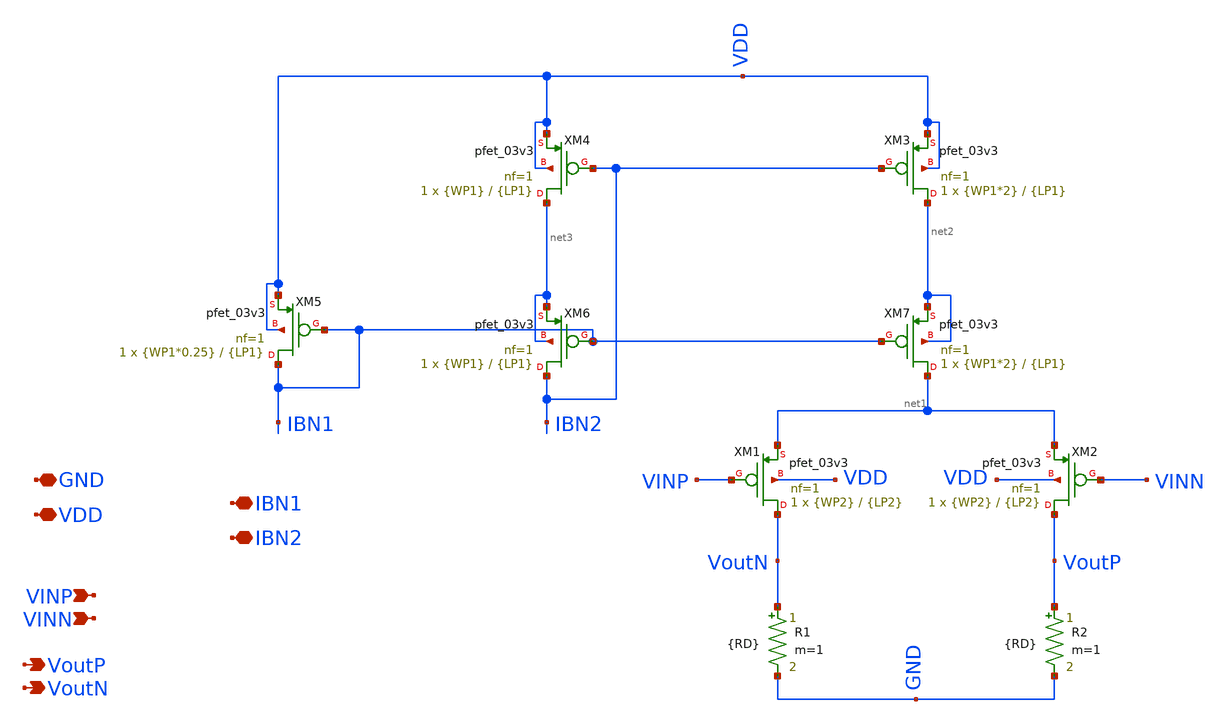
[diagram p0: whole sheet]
** sch_path: Lab_06/Diff_pair.sch
**.subckt Diff_pair IBN1 VINP VoutP VINN VDD GND VoutN IBN2
*.iopin IBN1
*.ipin VINP
*.opin VoutP
*.ipin VINN
*.iopin VDD
*.iopin GND
*.opin VoutN
*.iopin IBN2
XM1 VoutN VINP net1 VDD pfet_03v3 L={LP2} W={WP2} nf=1 ad='int((nf+1)/2) * W/nf * 0.18u' as='int((nf+2)/2) * W/nf * 0.18u'
+ pd='2*int((nf+1)/2) * (W/nf + 0.18u)' ps='2*int((nf+2)/2) * (W/nf + 0.18u)' nrd='0.18u / W' nrs='0.18u / W'
+ sa=0 sb=0 sd=0 m=1
XM2 VoutP VINN net1 VDD pfet_03v3 L={LP2} W={WP2} nf=1 ad='int((nf+1)/2) * W/nf * 0.18u' as='int((nf+2)/2) * W/nf * 0.18u'
+ pd='2*int((nf+1)/2) * (W/nf + 0.18u)' ps='2*int((nf+2)/2) * (W/nf + 0.18u)' nrd='0.18u / W' nrs='0.18u / W'
+ sa=0 sb=0 sd=0 m=1
XM3 net2 IBN2 VDD VDD pfet_03v3 L={LP1} W={WP1*2} nf=1 ad='int((nf+1)/2) * W/nf * 0.18u' as='int((nf+2)/2) * W/nf * 0.18u'
+ pd='2*int((nf+1)/2) * (W/nf + 0.18u)' ps='2*int((nf+2)/2) * (W/nf + 0.18u)' nrd='0.18u / W' nrs='0.18u / W'
+ sa=0 sb=0 sd=0 m=1
XM4 net3 IBN2 VDD VDD pfet_03v3 L={LP1} W={WP1} nf=1 ad='int((nf+1)/2) * W/nf * 0.18u' as='int((nf+2)/2) * W/nf * 0.18u'
+ pd='2*int((nf+1)/2) * (W/nf + 0.18u)' ps='2*int((nf+2)/2) * (W/nf + 0.18u)' nrd='0.18u / W' nrs='0.18u / W'
+ sa=0 sb=0 sd=0 m=1
R2 VoutP GND {RD} m=1
R1 VoutN GND {RD} m=1
XM5 IBN1 IBN1 VDD VDD pfet_03v3 L={LP1} W={WP1*0.25} nf=1 ad='int((nf+1)/2) * W/nf * 0.18u' as='int((nf+2)/2) * W/nf * 0.18u'
+ pd='2*int((nf+1)/2) * (W/nf + 0.18u)' ps='2*int((nf+2)/2) * (W/nf + 0.18u)' nrd='0.18u / W' nrs='0.18u / W'
+ sa=0 sb=0 sd=0 m=1
XM6 IBN2 IBN1 net3 net3 pfet_03v3 L={LP1} W={WP1} nf=1 ad='int((nf+1)/2) * W/nf * 0.18u' as='int((nf+2)/2) * W/nf * 0.18u'
+ pd='2*int((nf+1)/2) * (W/nf + 0.18u)' ps='2*int((nf+2)/2) * (W/nf + 0.18u)' nrd='0.18u / W' nrs='0.18u / W'
+ sa=0 sb=0 sd=0 m=1
XM7 net1 IBN1 net2 net2 pfet_03v3 L={LP1} W={WP1*2} nf=1 ad='int((nf+1)/2) * W/nf * 0.18u' as='int((nf+2)/2) * W/nf * 0.18u'
+ pd='2*int((nf+1)/2) * (W/nf + 0.18u)' ps='2*int((nf+2)/2) * (W/nf + 0.18u)' nrd='0.18u / W' nrs='0.18u / W'
+ sa=0 sb=0 sd=0 m=1
**.ends
.end
